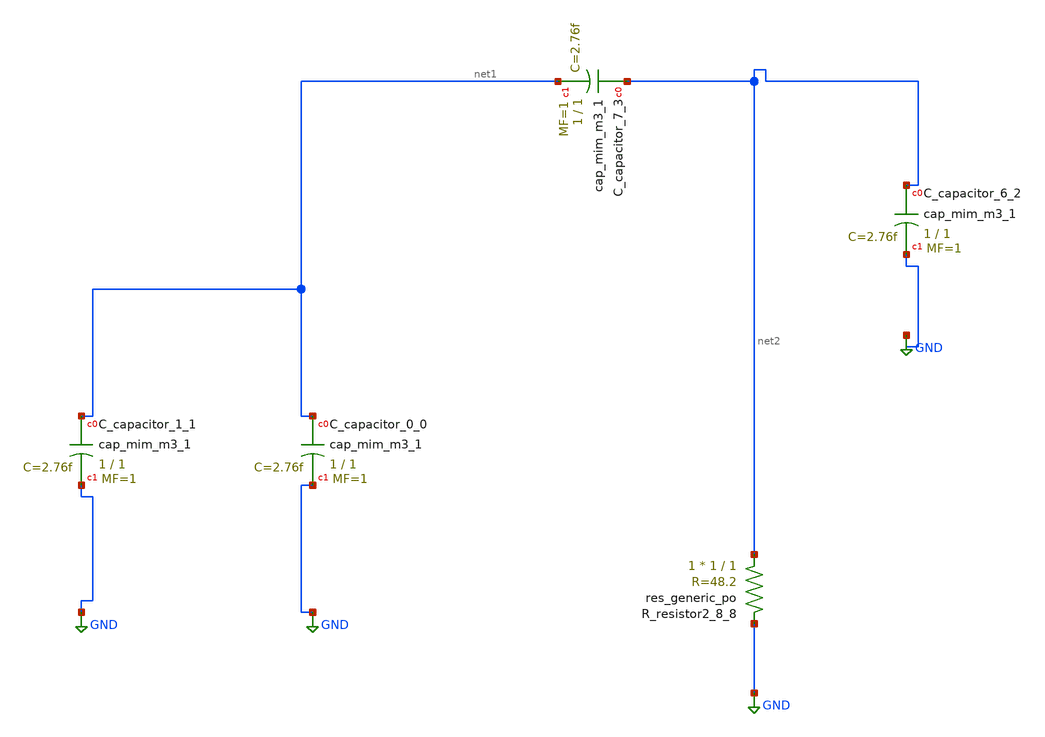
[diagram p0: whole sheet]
** sch_path: schematics/AMSNet/756.sch
**.subckt 756
XC_capacitor_0_0 net1 GND sky130_fd_pr__cap_mim_m3_1 W=1 L=1 MF=1 m=1
XC_capacitor_1_1 net1 GND sky130_fd_pr__cap_mim_m3_1 W=1 L=1 MF=1 m=1
XC_capacitor_6_2 net2 GND sky130_fd_pr__cap_mim_m3_1 W=1 L=1 MF=1 m=1
XC_capacitor_7_3 net2 net1 sky130_fd_pr__cap_mim_m3_1 W=1 L=1 MF=1 m=1
XR_resistor2_8_8 net2 GND sky130_fd_pr__res_generic_po W=1 L=1 m=1
**.ends
.GLOBAL GND
.end
